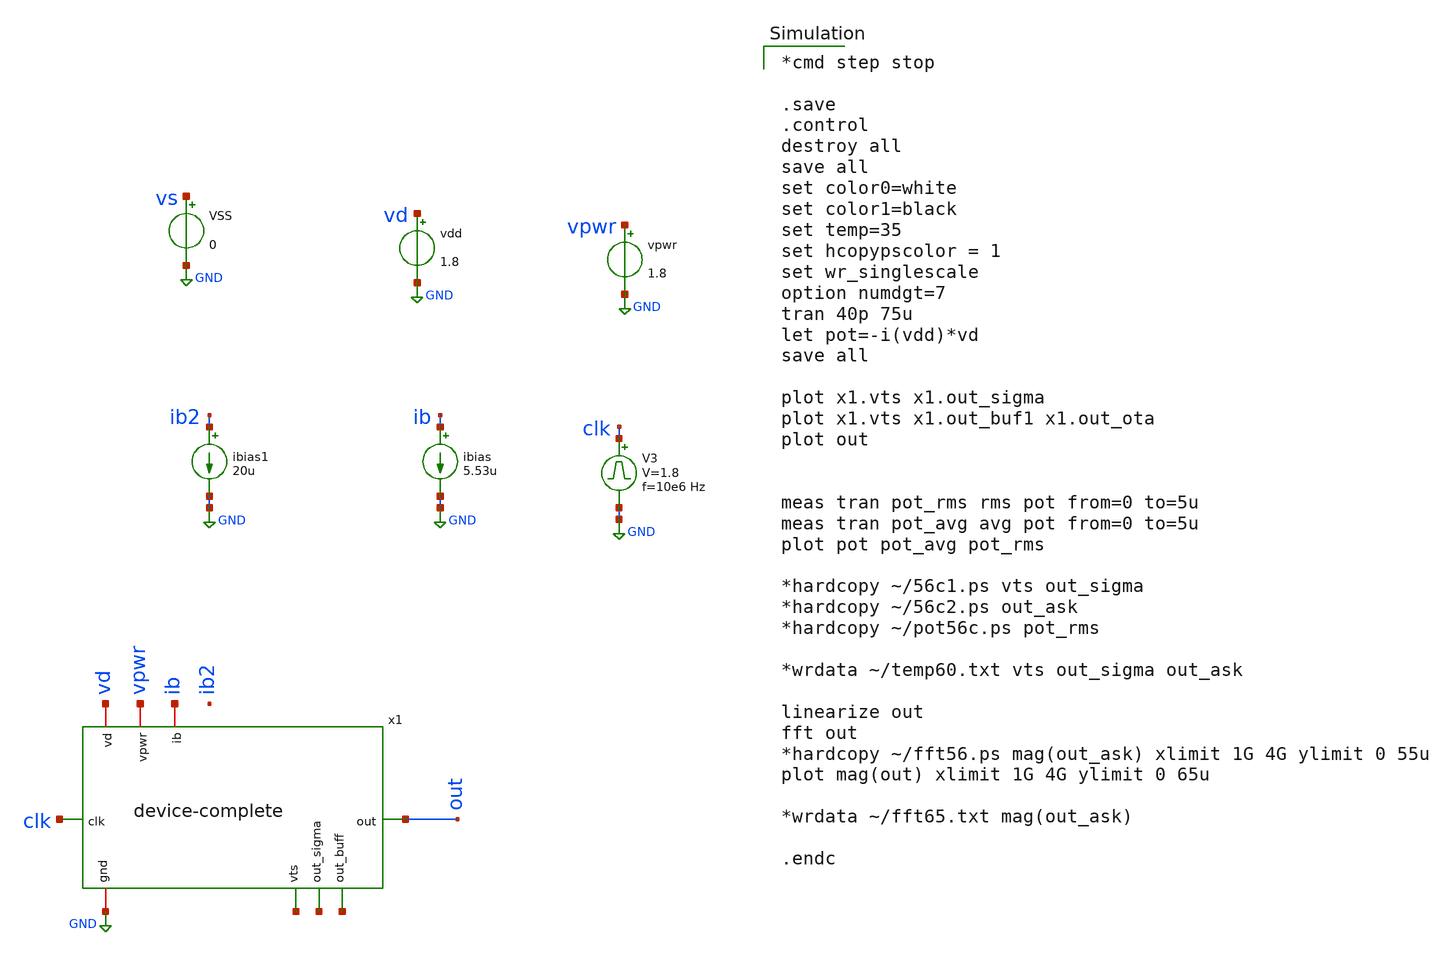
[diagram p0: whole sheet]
** sch_path: device-complete/xschem/device-complete-tb.sch
**.subckt device-complete-tb
vpwr vpwr GND 1.8
V3 clk GND pulse 0 1.8 '0.495/ 10e6 ' '0.01/10e6 ' '0.01/10e6 ' '0.49/10e6 ' '1/10e6 '
vdd vd GND 1.8
ibias ib GND 5.53u
VSS vs GND 0
ibias1 ib2 GND 20u
x1 vd clk out vpwr ib GND net1 net2 net3 device-complete
**** begin user architecture code

*cmd step stop

.save
.control
destroy all
save all
set color0=white
set color1=black
set temp=35
set hcopypscolor = 1
set wr_singlescale
option numdgt=7
tran 40p 75u
let pot=-i(vdd)*vd
save all

plot x1.vts x1.out_sigma
plot x1.vts x1.out_buf1 x1.out_ota
plot out


meas tran pot_rms rms pot from=0 to=5u
meas tran pot_avg avg pot from=0 to=5u
plot pot pot_avg pot_rms

*hardcopy ~/56c1.ps vts out_sigma
*hardcopy ~/56c2.ps out_ask
*hardcopy ~/pot56c.ps pot_rms

*wrdata ~/temp60.txt vts out_sigma out_ask

linearize out
fft out
*hardcopy ~/fft56.ps mag(out_ask) xlimit 1G 4G ylimit 0 55u
plot mag(out) xlimit 1G 4G ylimit 0 65u

*wrdata ~/fft65.txt mag(out_ask)

.endc



 .lib $::SKYWATER_MODELS/sky130.lib.spice tt
.include $::SKYWATER_STDCELLS/sky130_fd_sc_hd.spice

**** end user architecture code
**.ends
.GLOBAL GND
.end
